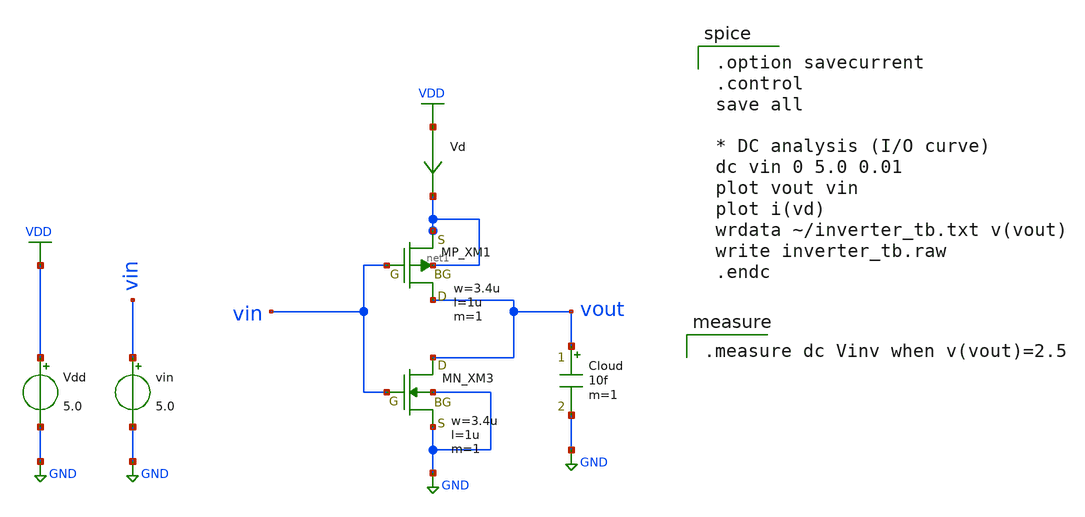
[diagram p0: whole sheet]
** sch_path: inverter/inverter_YU_WENJUN_tb.sch
**.subckt inverter_YU_WENJUN_tb
XXM1 vout vin net1 net1 PMOS w=3.4u l=1u nrd=0 nrs=0 m=1
Vdd VDD GND 5.0
vin vin GND 5.0
Vd VDD net1 0
.save i(vd)
Cloud vout GND 10f m=1
XXM3 vout vin GND GND NMOS w=3.4u l=1u nrd=0 nrs=0 m=1
**** begin user architecture code
 .include $::LIB/ip62_models

.option savecurrent
.control
save all

* DC analysis (I/O curve)
dc vin 0 5.0 0.01
plot vout vin
plot i(vd)
wrdata ~/inverter_tb.txt v(vout)
write inverter_tb.raw
.endc


.measure dc Vinv when v(vout)=2.5

**** end user architecture code
**.ends
.GLOBAL VDD
.GLOBAL GND
.end
